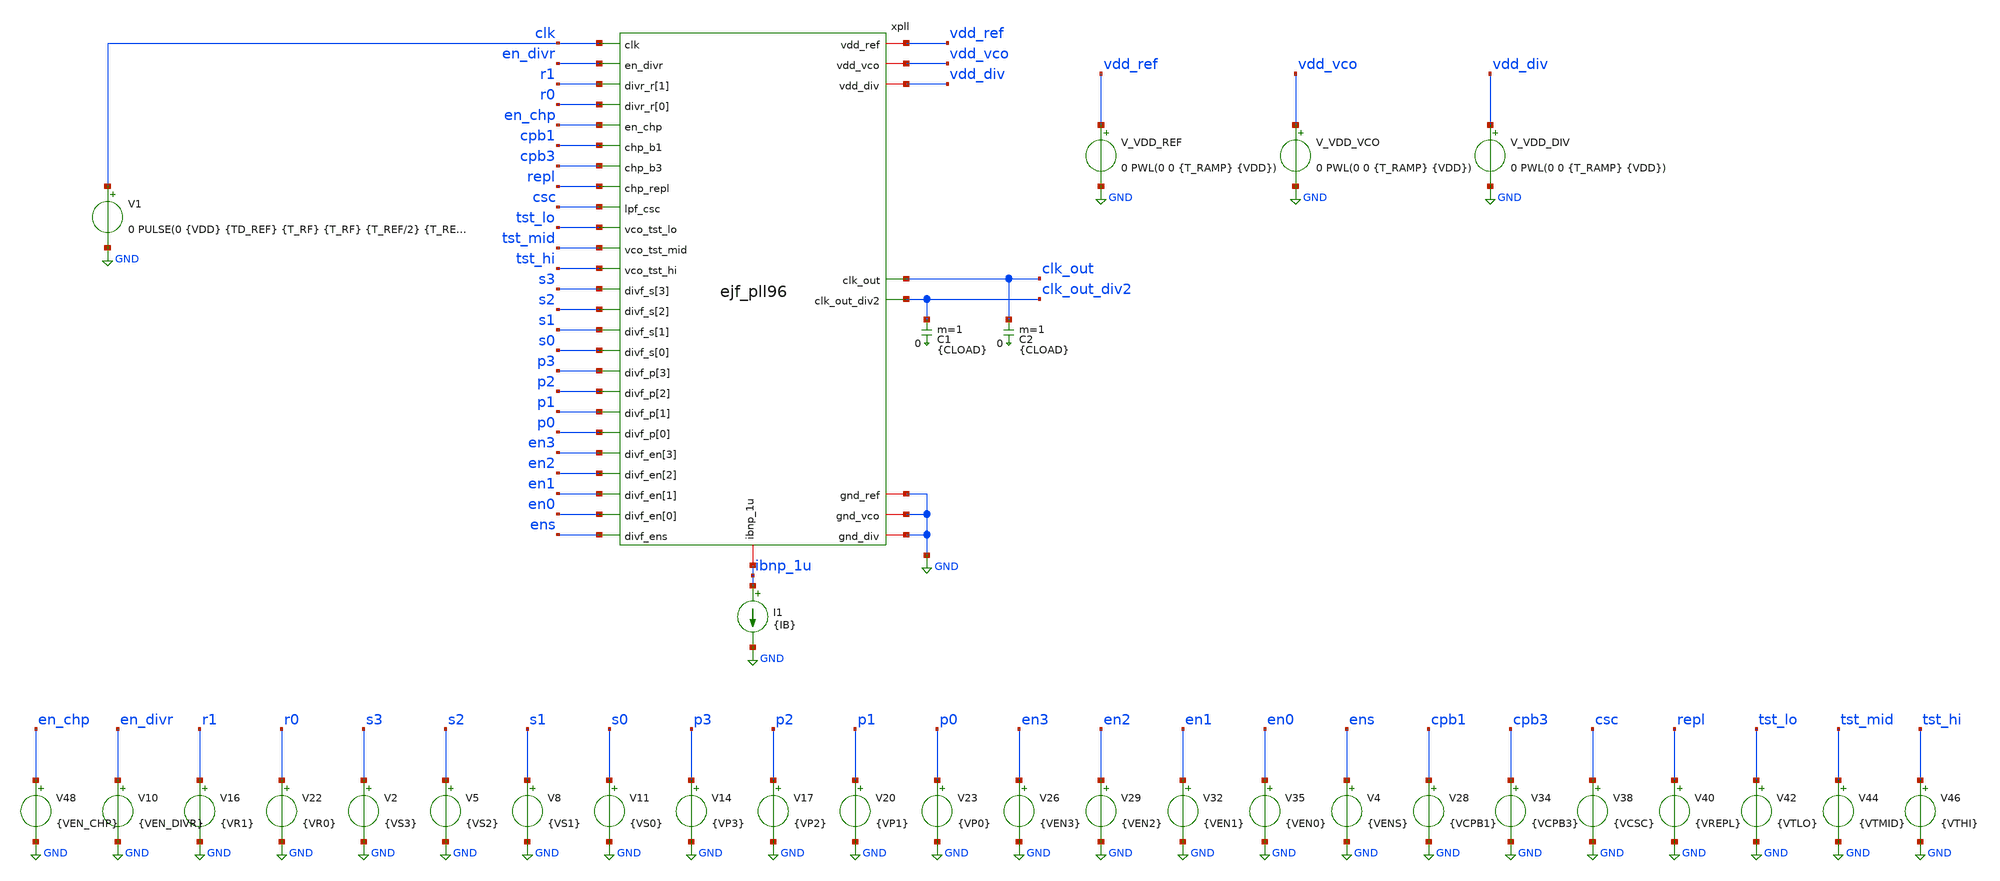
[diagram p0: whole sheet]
** sch_path: xschem/tb_ejf_pll96_top.sch
**.subckt tb_ejf_pll96_top
V_VDD_REF vdd_ref GND 0 PWL(0 0 {T_RAMP} {VDD})
.save i(v_vdd_ref)
V1 clk GND 0 PULSE(0 {VDD} {TD_REF} {T_RF} {T_RF} {T_REF/2} {T_REF})
xpll vdd_vco vdd_ref vdd_div clk_out r1 clk_out_div2 r0 clk en_divr GND s3 s2 s1 s0 GND p3 p2
+ ibnp_1u cpb3 p1 tst_hi cpb1 p0 tst_mid repl en3 tst_lo en_chp en2 en1 csc en0 ens GND ejf_pll96
V_VDD_VCO vdd_vco GND 0 PWL(0 0 {T_RAMP} {VDD})
.save i(v_vdd_vco)
V_VDD_DIV vdd_div GND 0 PWL(0 0 {T_RAMP} {VDD})
.save i(v_vdd_div)
V2 s3 GND {VS3}
V5 s2 GND {VS2}
V8 s1 GND {VS1}
V11 s0 GND {VS0}
V14 p3 GND {VP3}
V17 p2 GND {VP2}
V20 p1 GND {VP1}
V23 p0 GND {VP0}
V26 en3 GND {VEN3}
V29 en2 GND {VEN2}
V32 en1 GND {VEN1}
V35 en0 GND {VEN0}
V4 ens GND {VENS}
I1 ibnp_1u GND {IB}
V10 en_divr GND {VEN_DIVR}
V16 r1 GND {VR1}
V22 r0 GND {VR0}
V28 cpb1 GND {VCPB1}
V34 cpb3 GND {VCPB3}
V38 csc GND {VCSC}
C1 clk_out_div2 0 {CLOAD} m=1
C2 clk_out 0 {CLOAD} m=1
V40 repl GND {VREPL}
V42 tst_lo GND {VTLO}
V44 tst_mid GND {VTMID}
V46 tst_hi GND {VTHI}
V48 en_chp GND {VEN_CHP}
**** begin user architecture code

* ejf_pfd test
.lib ~/.volare/sky130A/libs.tech/combined/sky130.lib.spice tt
.include ~/.volare/sky130A/libs.ref/sky130_fd_sc_ls/spice/sky130_fd_sc_ls.spice
.option temp=27
.param VDD=1.8
.param T_REF=200n
.param TD_REF=50n
.param T_RF=300p
.param T_RAMP=50n
.param CP=10f
.param CLOAD=100f
.param IB=1u
.param VEN_DIVR=1.8
.param VEN_CHP=1.8
.param VR0=0
.param VR1=0
.param VS3=0
.param VS2=1.8
.param VS1=0
.param VS0=0
.param VP3=0
.param VP2=1.8
.param VP1=1.8
.param VP0=1.8
.param VEN3=0
.param VEN2=1.8
.param VEN1=1.8
.param VEN0=1.8
.param VENS=1.8
.param VCPB1=1.8
.param VCPB3=0
.param VCSC=1.8
.param VREPL=1.8
.param VTLO=0
.param VTMID=0
.param VTHI=0



* Run transient
* default reltol=1e-3 vntol=1e-6 abstol=1e-12
.options  reltol=1e-4 vntol=1e-7 abstol=1e-13
.options klu
.control
   save i(v_vdd_ref) i(v_vdd_vco) i(v_vdd_div)
   save clk clk_out clk_out_div2 ibnp_1u
   save xpll.qref xpll.qref_b xpll.qclk xpll.qclk_b xpll.vc xpll.vco_outp xpll.vco_outn
   save xpll.xvco.vhi xpll.clk_divf
   save xpll.xvco.x0p xpll.xvco.x0n xpll.xvco.x1p xpll.xvco.x1n xpll.xvco.x2p xpll.xvco.x2n
+ xpll.xvco.x3p xpll.xvco.x3n
   save xpll.xchp.cp_repl xpll.xchp.mp1g xpll.xchp.mp1cg xpll.xchp.mn1g
   save xpll.xchp.mn1d xpll.xchp.mp1d
   save xpll.xlpf.mpc2g xpll.xlpf.bp
   tran 1n 30u
   write tb_ejf_pll96_top.raw
   meas tran idd_ref avg i(v_vdd_ref) from=18u to=20u
   meas tran idd_vco avg i(v_vdd_vco) from=18u to=20u
   meas tran idd_div avg i(v_vdd_div) from=18u to=20u
   plot xpll.vc
.endc
.end

**** end user architecture code
**.ends
.GLOBAL GND
.end
